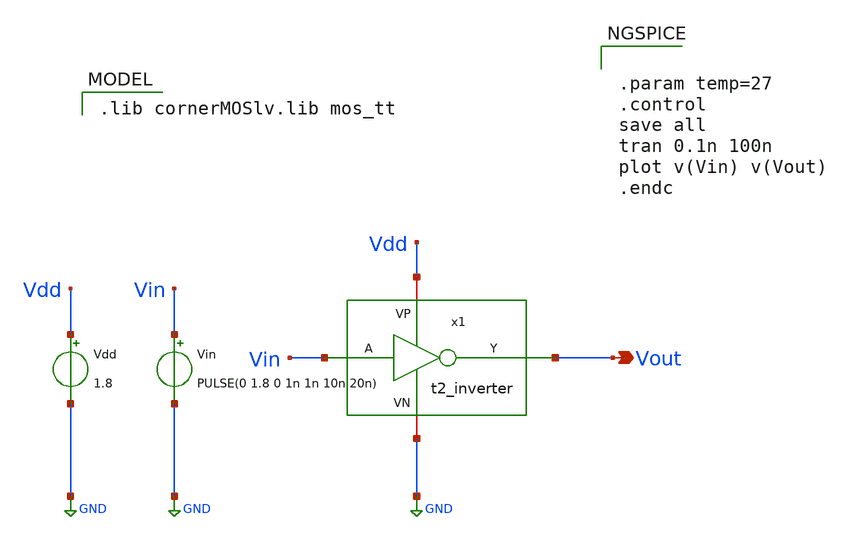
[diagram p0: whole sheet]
** sch_path: Team 2 Design/design_data/xschem/t2_inverter_tb_pulse.sch
**.subckt t2_inverter_tb_pulse Vout
*.opin Vout
Vin Vin GND PULSE(0 1.8 0 1n 1n 10n 20n)
Vdd Vdd GND 1.8
x1 Vdd Vin Vout GND t2_inverter
**** begin user architecture code
 .lib cornerMOSlv.lib mos_tt



.param temp=27
.control
save all
tran 0.1n 100n
plot v(Vin) v(Vout)
.endc


**** end user architecture code
**.ends

* expanding   symbol:  /foss/designs/cmos-pll-ihp-sg13g2/Team 2
*+ Design/design_data/xschem/t2_inverter.sym # of pins=4
** sym_path: Team 2 Design/design_data/xschem/t2_inverter.sym
** sch_path: Team 2 Design/design_data/xschem/t2_inverter.sch
.subckt t2_inverter VP A Y VN
*.iopin VP
*.iopin VN
*.ipin A
*.opin Y
XM2 Y A VP VP sg13_lv_pmos w=0.3u l=0.13u ng=1 m=1 mm_ok=1
XM1 Y A VN VN sg13_lv_nmos w=0.15u l=0.13u ng=1 m=1 mm_ok=1
.ends

.GLOBAL GND
.end
